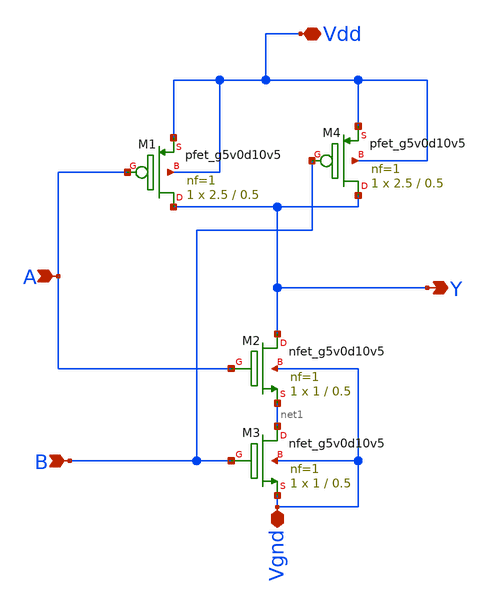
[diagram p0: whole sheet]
** sch_path: sky130_cells/RDAC/Design/sky130_hilas_2NAND.sch
**.subckt sky130_hilas_2NAND Vgnd Vdd A B Y
*.iopin Vgnd
*.iopin Vdd
*.ipin A
*.ipin B
*.opin Y
XM1 Y A Vdd Vdd sky130_fd_pr__pfet_g5v0d10v5 L=0.5 W=2.5 nf=1 ad='int((nf+1)/2) * W/nf * 0.29' as='int((nf+2)/2) * W/nf * 0.29'
+ pd='2*int((nf+1)/2) * (W/nf + 0.29)' ps='2*int((nf+2)/2) * (W/nf + 0.29)' nrd='0.29 / W' nrs='0.29 / W'
+ sa=0 sb=0 sd=0 mult=1 m=1
XM2 Y A net1 Vgnd sky130_fd_pr__nfet_g5v0d10v5 L=0.5 W=1 nf=1 ad='int((nf+1)/2) * W/nf * 0.29' as='int((nf+2)/2) * W/nf * 0.29'
+ pd='2*int((nf+1)/2) * (W/nf + 0.29)' ps='2*int((nf+2)/2) * (W/nf + 0.29)' nrd='0.29 / W' nrs='0.29 / W'
+ sa=0 sb=0 sd=0 mult=1 m=1
XM3 net1 B Vgnd Vgnd sky130_fd_pr__nfet_g5v0d10v5 L=0.5 W=1 nf=1 ad='int((nf+1)/2) * W/nf * 0.29' as='int((nf+2)/2) * W/nf * 0.29'
+ pd='2*int((nf+1)/2) * (W/nf + 0.29)' ps='2*int((nf+2)/2) * (W/nf + 0.29)' nrd='0.29 / W' nrs='0.29 / W'
+ sa=0 sb=0 sd=0 mult=1 m=1
XM4 Y B Vdd Vdd sky130_fd_pr__pfet_g5v0d10v5 L=0.5 W=2.5 nf=1 ad='int((nf+1)/2) * W/nf * 0.29' as='int((nf+2)/2) * W/nf * 0.29'
+ pd='2*int((nf+1)/2) * (W/nf + 0.29)' ps='2*int((nf+2)/2) * (W/nf + 0.29)' nrd='0.29 / W' nrs='0.29 / W'
+ sa=0 sb=0 sd=0 mult=1 m=1
**.ends
.end
